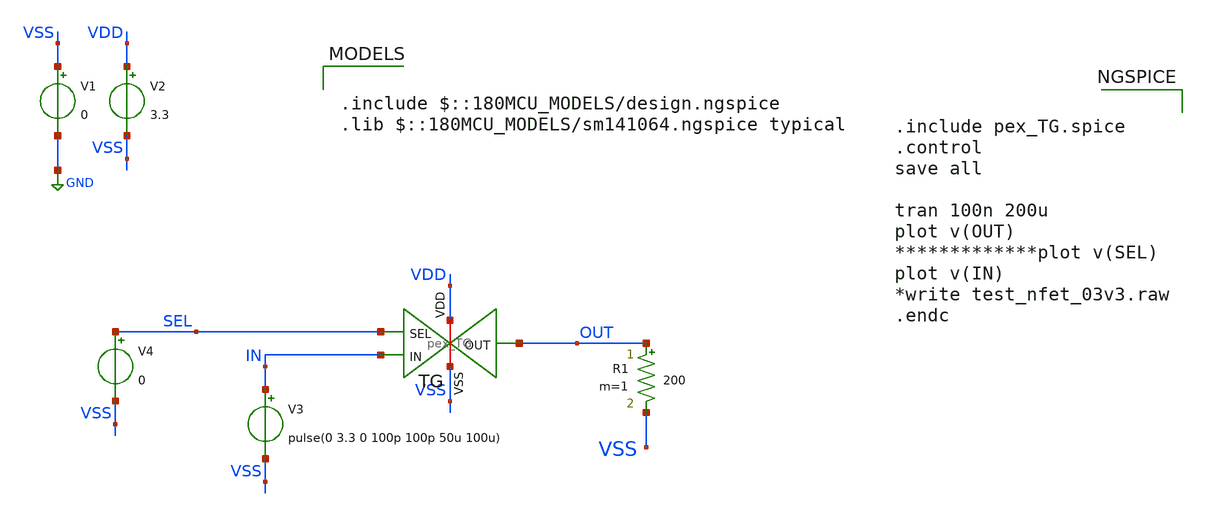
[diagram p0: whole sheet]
** sch_path: DAC_PAKISTAN_01/Pakistan1_Xschem/TG_TB.sch
**.subckt TG_TB
V1 VSS GND 0
V2 VDD VSS 3.3
V3 IN VSS pulse(0 3.3 0 100p 100p 50u 100u)
V4 SEL VSS 0
x1 VDD SEL VSS OUT IN pex_TG
R1 OUT VSS 200 m=1
**** begin user architecture code

.include $::180MCU_MODELS/design.ngspice
.lib $::180MCU_MODELS/sm141064.ngspice typical



.include pex_TG.spice
.control
save all

tran 100n 200u
plot v(OUT)
*************plot v(SEL)
plot v(IN)
*write test_nfet_03v3.raw
.endc


**** end user architecture code
**.ends
.GLOBAL GND
.end
